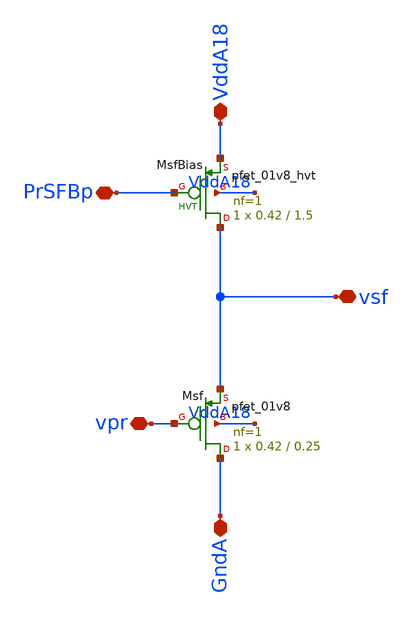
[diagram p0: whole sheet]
** sch_path: analog/klayout/production/final_merge_20260923/testbenches/cace/analog/xschem/PixelSourceFollower.sch
**.subckt PixelSourceFollower GndA PrSFBp vpr vsf VddA18
*.iopin GndA
*.iopin PrSFBp
*.iopin vpr
*.iopin vsf
*.iopin VddA18
XMsfBias vsf PrSFBp VddA18 VddA18 sky130_fd_pr__pfet_01v8_hvt L=1.5 W=0.42 nf=1 ad='int((1 + 1)/2) * 0.42 / 1 * 0.29'
+ as='int((1 + 2)/2) * 0.42 / 1 * 0.29' pd='2*int((1 + 1)/2) * (0.42 / 1 + 0.29)' ps='2*int((1 + 2)/2) * (0.42 / 1 + 0.29)'
+ nrd='0.29 / 0.42 ' nrs='0.29 / 0.42 ' sa=0 sb=0 sd=0 mult=1 m=1
XMsf GndA vpr vsf VddA18 sky130_fd_pr__pfet_01v8 L=0.25 W=0.42 nf=1 ad='int((1 + 1)/2) * 0.42 / 1 * 0.29'
+ as='int((1 + 2)/2) * 0.42 / 1 * 0.29' pd='2*int((1 + 1)/2) * (0.42 / 1 + 0.29)' ps='2*int((1 + 2)/2) * (0.42 / 1 + 0.29)'
+ nrd='0.29 / 0.42 ' nrs='0.29 / 0.42 ' sa=0 sb=0 sd=0 mult=1 m=1
**.ends
.end
